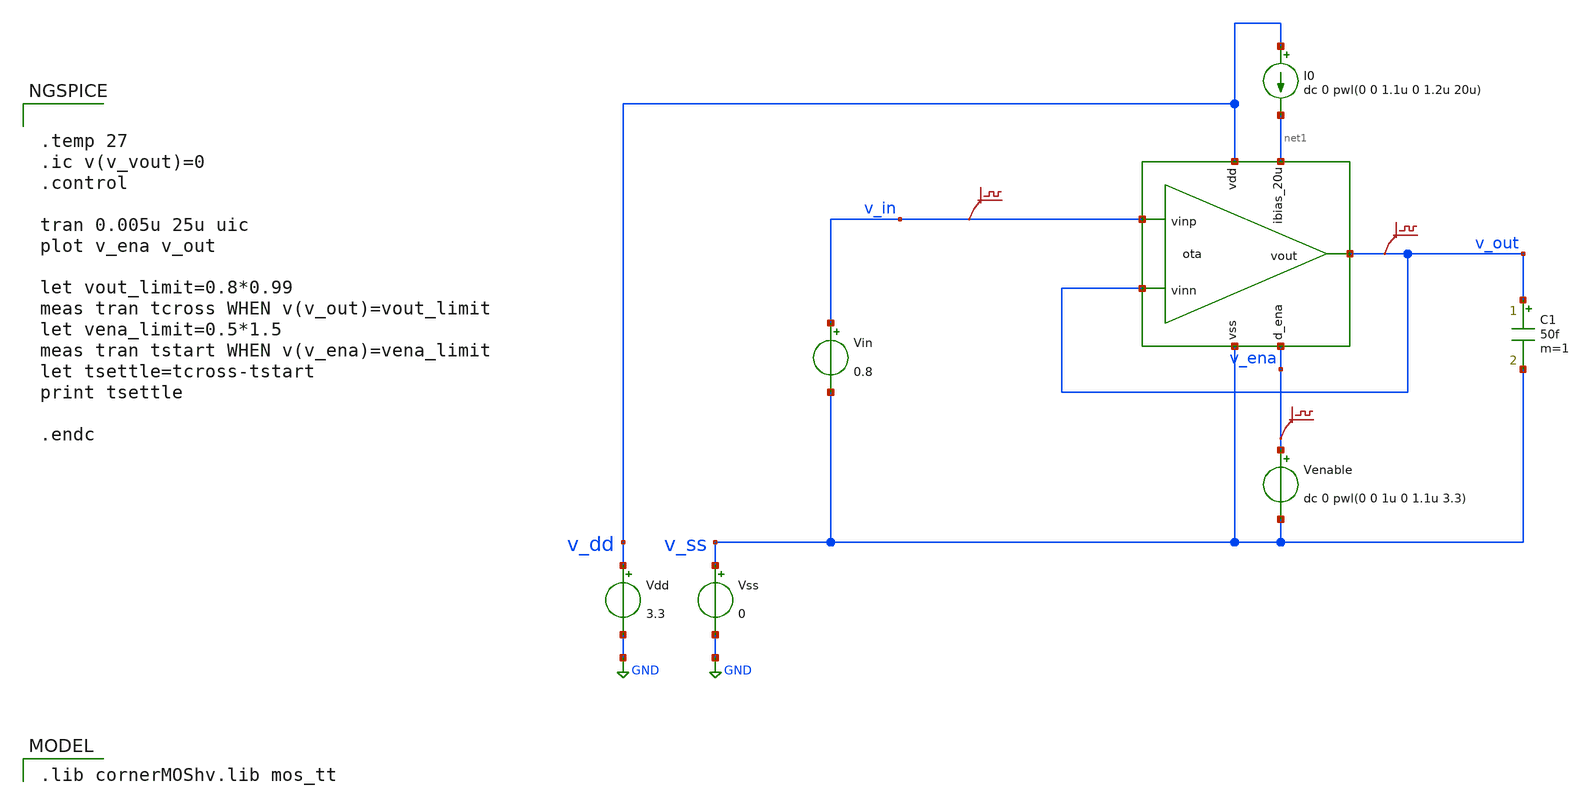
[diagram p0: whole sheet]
** sch_path: Differntial_Amp/design_data/xschem/ota-5t_tb-tran.sch
* Copyright 2024 Harald Pretl
**.subckt ota-5t_tb-tran
Vdd v_dd GND 3.3
Vss v_ss GND 0
C1 v_out v_ss 50f m=1
Vin v_in v_ss 0.8
I0 v_dd net1 dc 0 pwl(0 0 1.1u 0 1.2u 20u)
Venable v_ena v_ss dc 0 pwl(0 0 1u 0 1.1u 3.3)
.save v(v_in)
.save v(v_out)
.save v(v_ena)
x1 v_dd v_out v_in v_out net1 v_ss v_ena ota
**** begin user architecture code
 .lib cornerMOShv.lib mos_tt



.temp 27
.ic v(v_vout)=0
.control

tran 0.005u 25u uic
plot v_ena v_out

let vout_limit=0.8*0.99
meas tran tcross WHEN v(v_out)=vout_limit
let vena_limit=0.5*1.5
meas tran tstart WHEN v(v_ena)=vena_limit
let tsettle=tcross-tstart
print tsettle

.endc


**** end user architecture code
**.ends

* expanding   symbol:
*+  /home/aidas93/Downloads/TO_Nov2024-main/Differntial_Amp/design_data/xschem/ota.sym # of pins=7
** sym_path: Differntial_Amp/design_data/xschem/ota.sym
** sch_path: Differntial_Amp/design_data/xschem/ota.sch
.subckt ota vdd vout vinp vinn ibias_20u vss d_ena
*.opin vout
*.iopin vdd
*.iopin vss
*.ipin ibias_20u
*.ipin vinn
*.ipin vinp
*.ipin d_ena
XM1 vout vinn net2 vss sg13_hv_nmos w=0.53u l=1u ng=1 m=4 mm_ok=1
XM2 net1 vinp net2 vss sg13_hv_nmos w=0.53u l=1u ng=1 m=4 mm_ok=1
XM5 net2 net3 vss vss sg13_hv_nmos w=0.76u l=1u ng=1 m=1 mm_ok=1
XM3 net1 net1 vdd vdd sg13_hv_pmos w=1.45u l=1u ng=1 m=1 mm_ok=1
XM4 vout net1 vdd vdd sg13_hv_pmos w=1.45u l=1u ng=1 m=1 mm_ok=1
XM6 ibias_20u net3 vss vss sg13_hv_nmos w=3.075u l=1u ng=5 m=1 mm_ok=1
XM7 net1 d_ena vdd vdd sg13_hv_pmos w=1.5u l=1u ng=1 m=1 mm_ok=1
XM8 net4 d_ena vdd vdd sg13_hv_pmos w=1.5u l=1u ng=1 m=1 mm_ok=1
XM9 ibias_20u net4 net3 vss sg13_hv_nmos w=0.5u l=1u ng=1 m=1 mm_ok=1
XM10 net3 net4 vss vss sg13_hv_nmos w=0.5u l=1u ng=1 m=1 mm_ok=1
XM11 net4 d_ena vss vss sg13_hv_nmos w=0.5u l=1u ng=1 m=1 mm_ok=1
XM12 vss vss vss vss sg13_hv_nmos w=0.5u l=0.5u ng=1 m=1 mm_ok=1
XM13 vss vss vss vss sg13_hv_nmos w=0.5u l=0.5u ng=1 m=1 mm_ok=1
XM14 vss vss vss vss sg13_hv_nmos w=0.76u l=0.5u ng=1 m=1 mm_ok=1
XM15 vss vss vss vss sg13_hv_nmos w=0.615u l=0.5u ng=1 m=1 mm_ok=1
XM16 vss vss vss vss sg13_hv_nmos w=0.615u l=0.5u ng=1 m=1 mm_ok=1
XM17 vss vss vss vss sg13_hv_nmos w=0.76u l=0.5u ng=1 m=1 mm_ok=1
XM18 vss vss vss vss sg13_hv_nmos w=0.5u l=0.5u ng=1 m=1 mm_ok=1
XM19 vss vss vss vss sg13_hv_nmos w=0.5u l=0.5u ng=1 m=1 mm_ok=1
XM20 vss vss vss vss sg13_hv_nmos w=0.53u l=0.5u ng=1 m=1 mm_ok=1
XM21 vss vss vss vss sg13_hv_nmos w=0.53u l=0.5u ng=1 m=1 mm_ok=1
XM22 vss vss vss vss sg13_hv_nmos w=0.53u l=0.5u ng=1 m=1 mm_ok=1
XM23 vss vss vss vss sg13_hv_nmos w=0.53u l=0.5u ng=1 m=1 mm_ok=1
XM24 vss vss vss vss sg13_hv_nmos w=0.5u l=1u ng=1 m=1 mm_ok=1
XM25 vss vss vss vss sg13_hv_nmos w=0.5u l=1u ng=1 m=1 mm_ok=1
XM26 vss vss vss vss sg13_hv_nmos w=0.5u l=0.5u ng=1 m=1 mm_ok=1
XM27 vss vss vss vss sg13_hv_nmos w=0.5u l=0.5u ng=1 m=1 mm_ok=1
XM28 vss vss vss vss sg13_hv_nmos w=0.53u l=0.5u ng=1 m=1 mm_ok=1
XM29 vss vss vss vss sg13_hv_nmos w=0.53u l=0.5u ng=1 m=1 mm_ok=1
XM30 vss vss vss vss sg13_hv_nmos w=0.53u l=0.5u ng=1 m=1 mm_ok=1
XM31 vss vss vss vss sg13_hv_nmos w=0.53u l=0.5u ng=1 m=1 mm_ok=1
XM32 vss vss vss vss sg13_hv_nmos w=0.5u l=1u ng=1 m=1 mm_ok=1
XM33 vss vss vss vss sg13_hv_nmos w=0.5u l=1u ng=1 m=1 mm_ok=1
XM34 vdd vdd vdd vdd sg13_hv_pmos w=1.45u l=0.5u ng=1 m=1 mm_ok=1
XM35 vdd vdd vdd vdd sg13_hv_pmos w=1.45u l=0.5u ng=1 m=1 mm_ok=1
XM36 vdd vdd vdd vdd sg13_hv_pmos w=1.45u l=0.5u ng=1 m=1 mm_ok=1
XM37 vdd vdd vdd vdd sg13_hv_pmos w=1.45u l=0.5u ng=1 m=1 mm_ok=1
.ends

.GLOBAL GND
.end
